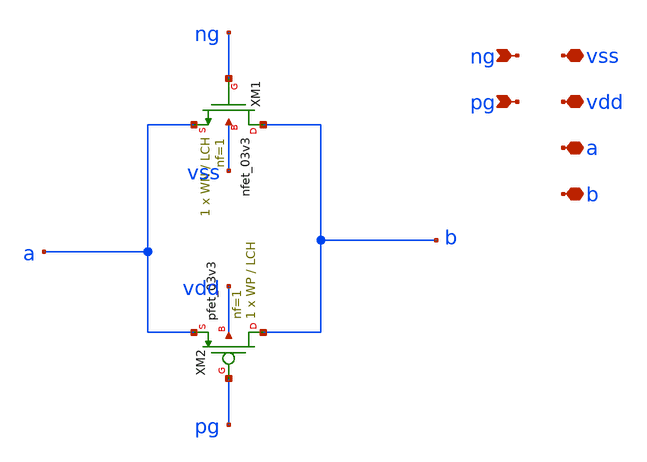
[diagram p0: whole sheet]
** sch_path: circuit_files/xschem/tg_param.sch
**.subckt tg_param ng vdd pg a b vss
*.ipin ng
*.iopin vdd
*.ipin pg
*.iopin a
*.iopin b
*.iopin vss
XM2 b pg a vdd pfet_03v3 L=LCH W=WP nf=1 ad='int((nf+1)/2) * W/nf * 0.18u' as='int((nf+2)/2) * W/nf * 0.18u'
+ pd='2*int((nf+1)/2) * (W/nf + 0.18u)' ps='2*int((nf+2)/2) * (W/nf + 0.18u)' nrd='0.18u / W' nrs='0.18u / W'
+ sa=0 sb=0 sd=0 m=1
XM1 b ng a vss nfet_03v3 L=LCH W=WN nf=1 ad='int((nf+1)/2) * W/nf * 0.18u' as='int((nf+2)/2) * W/nf * 0.18u'
+ pd='2*int((nf+1)/2) * (W/nf + 0.18u)' ps='2*int((nf+2)/2) * (W/nf + 0.18u)' nrd='0.18u / W' nrs='0.18u / W'
+ sa=0 sb=0 sd=0 m=1
**.ends
.end
